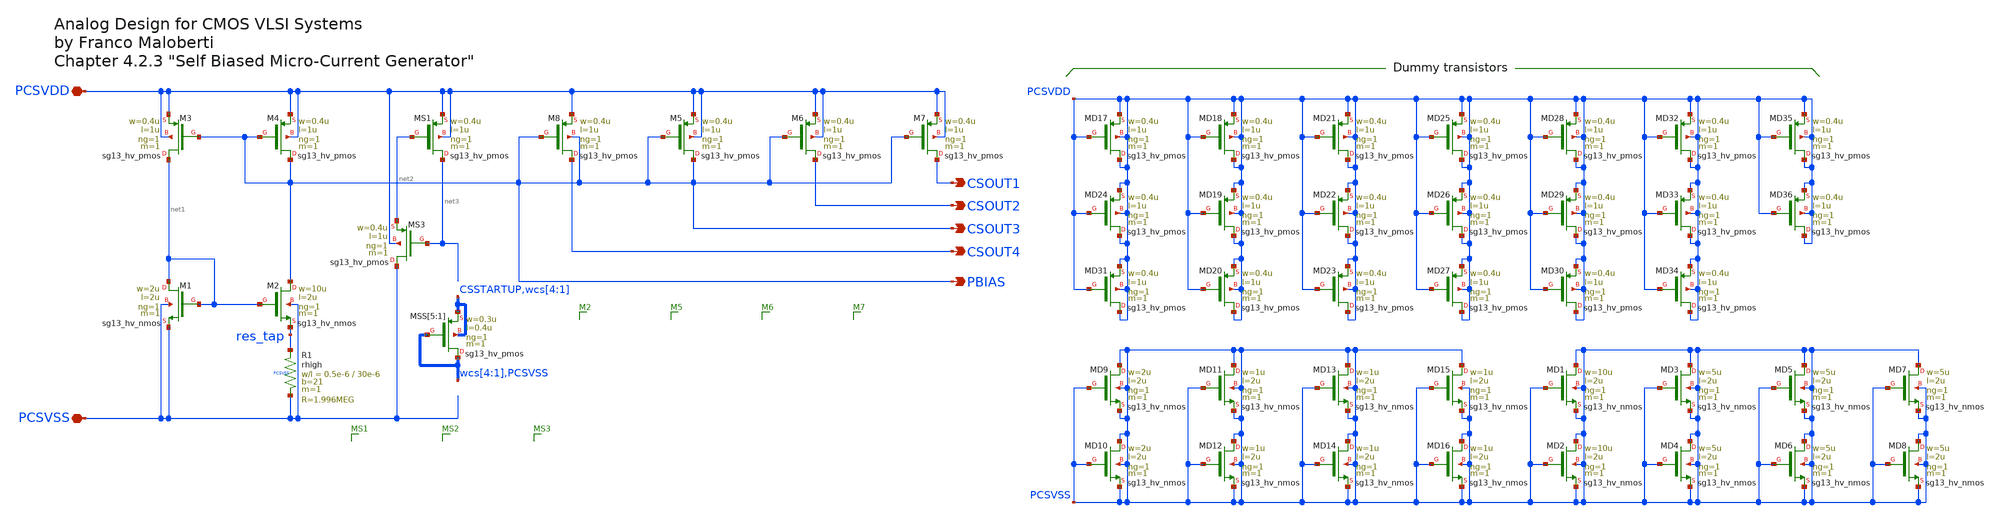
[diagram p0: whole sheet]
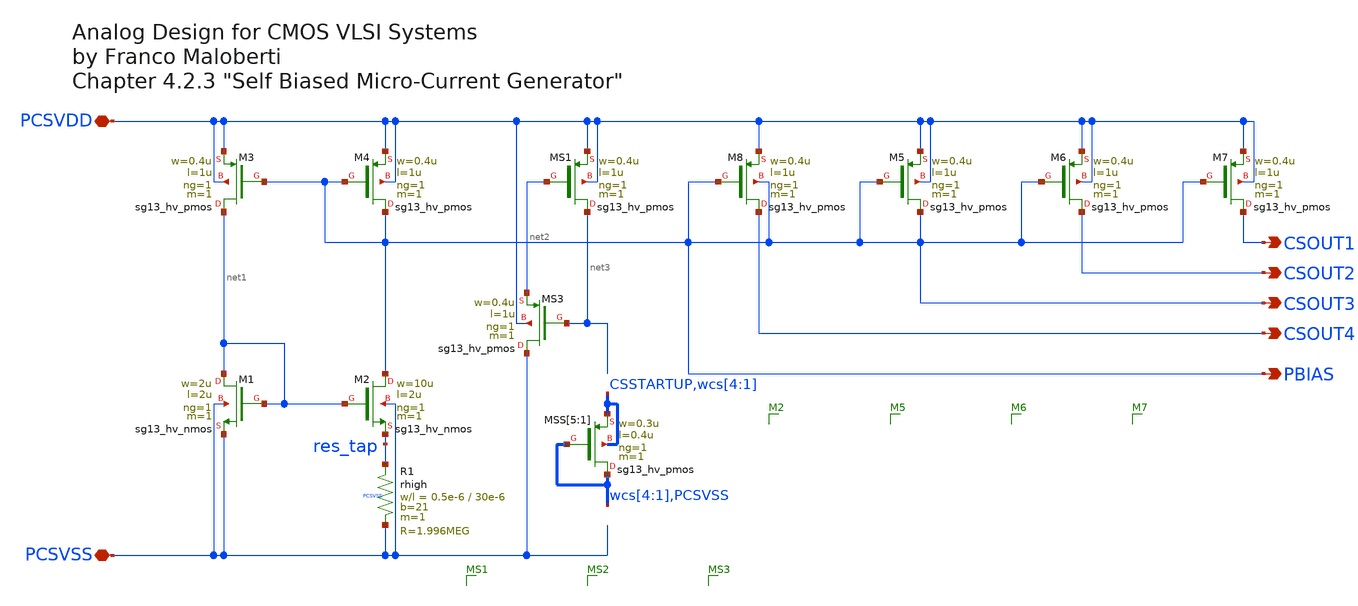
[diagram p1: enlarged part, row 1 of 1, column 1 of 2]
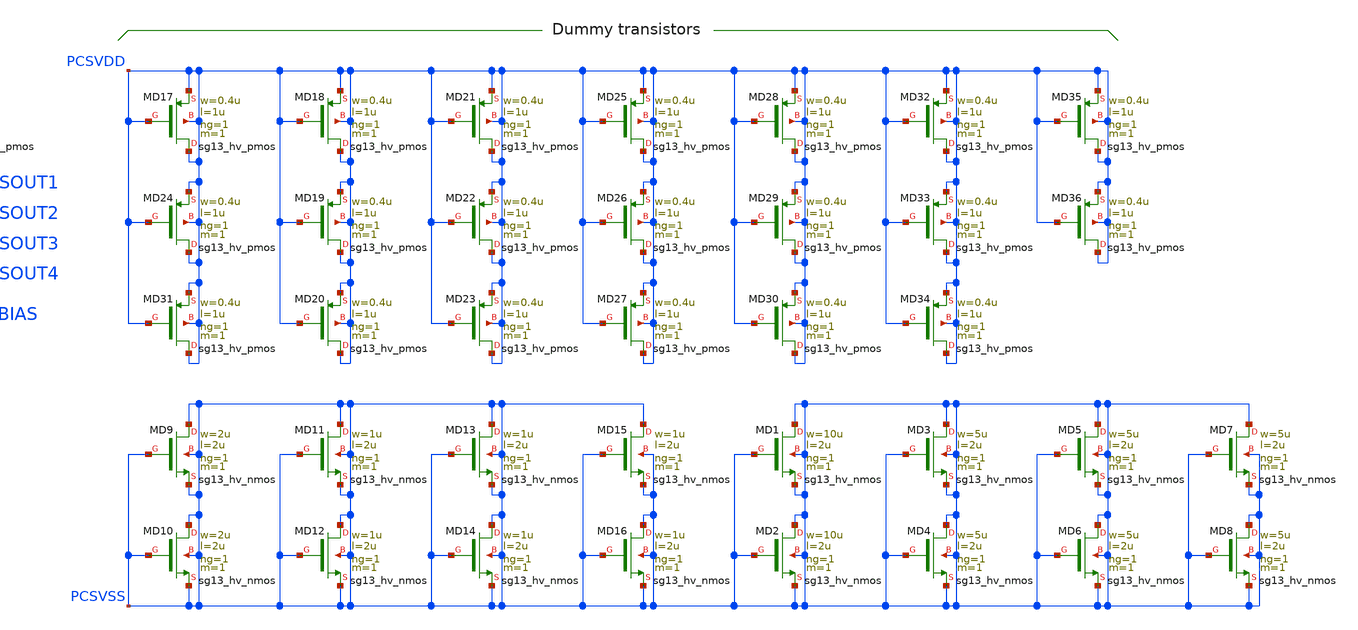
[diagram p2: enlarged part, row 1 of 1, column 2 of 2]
** sch_path: macros/heichips26_FAIf/macros/ptat_current_source/schematic/xschem/ptat_curr_gen_mod1.sch
**.subckt ptat_curr_gen_mod1 PCSVDD PCSVSS CSOUT1 CSOUT2 CSOUT3 PBIAS CSOUT4
*.iopin PCSVDD
*.iopin PCSVSS
*.opin CSOUT1
*.opin CSOUT2
*.opin CSOUT3
*.opin PBIAS
*.opin CSOUT4
XM1 net1 net1 PCSVSS PCSVSS sg13_hv_nmos w=2u l=2u ng=1 m=1 mm_ok=1
XM2 CSOUT3 net1 res_tap PCSVSS sg13_hv_nmos w=10u l=2u ng=1 m=1 mm_ok=1
XM3 net1 CSOUT3 PCSVDD PCSVDD sg13_hv_pmos w=0.4u l=1u ng=1 m=1 mm_ok=1
XM4 CSOUT3 CSOUT3 PCSVDD PCSVDD sg13_hv_pmos w=0.4u l=1u ng=1 m=1 mm_ok=1
XR1 res_tap PCSVSS PCSVSS rhigh w=0.5e-6 l=30e-6 m=1 b=21 mm_ok=1
XM5 CSOUT3 CSOUT3 PCSVDD PCSVDD sg13_hv_pmos w=0.4u l=1u ng=1 m=1 mm_ok=1
XM6 CSOUT2 CSOUT3 PCSVDD PCSVDD sg13_hv_pmos w=0.4u l=1u ng=1 m=1 mm_ok=1
XM7 CSOUT1 CSOUT3 PCSVDD PCSVDD sg13_hv_pmos w=0.4u l=1u ng=1 m=1 mm_ok=1
XMD1 PCSVSS PCSVSS PCSVSS PCSVSS sg13_hv_nmos w=10u l=2u ng=1 m=1 mm_ok=1
XMD2 PCSVSS PCSVSS PCSVSS PCSVSS sg13_hv_nmos w=10u l=2u ng=1 m=1 mm_ok=1
XMD3 PCSVSS PCSVSS PCSVSS PCSVSS sg13_hv_nmos w=5u l=2u ng=1 m=1 mm_ok=1
XMD4 PCSVSS PCSVSS PCSVSS PCSVSS sg13_hv_nmos w=5u l=2u ng=1 m=1 mm_ok=1
XMD5 PCSVSS PCSVSS PCSVSS PCSVSS sg13_hv_nmos w=5u l=2u ng=1 m=1 mm_ok=1
XMD6 PCSVSS PCSVSS PCSVSS PCSVSS sg13_hv_nmos w=5u l=2u ng=1 m=1 mm_ok=1
XMD7 PCSVSS PCSVSS PCSVSS PCSVSS sg13_hv_nmos w=5u l=2u ng=1 m=1 mm_ok=1
XMD8 PCSVSS PCSVSS PCSVSS PCSVSS sg13_hv_nmos w=5u l=2u ng=1 m=1 mm_ok=1
XMD9 PCSVSS PCSVSS PCSVSS PCSVSS sg13_hv_nmos w=2u l=2u ng=1 m=1 mm_ok=1
XMD10 PCSVSS PCSVSS PCSVSS PCSVSS sg13_hv_nmos w=2u l=2u ng=1 m=1 mm_ok=1
XMD11 PCSVSS PCSVSS PCSVSS PCSVSS sg13_hv_nmos w=1u l=2u ng=1 m=1 mm_ok=1
XMD12 PCSVSS PCSVSS PCSVSS PCSVSS sg13_hv_nmos w=1u l=2u ng=1 m=1 mm_ok=1
XMD13 PCSVSS PCSVSS PCSVSS PCSVSS sg13_hv_nmos w=1u l=2u ng=1 m=1 mm_ok=1
XMD14 PCSVSS PCSVSS PCSVSS PCSVSS sg13_hv_nmos w=1u l=2u ng=1 m=1 mm_ok=1
XMD15 PCSVSS PCSVSS PCSVSS PCSVSS sg13_hv_nmos w=1u l=2u ng=1 m=1 mm_ok=1
XMD16 PCSVSS PCSVSS PCSVSS PCSVSS sg13_hv_nmos w=1u l=2u ng=1 m=1 mm_ok=1
XMD17 PCSVDD PCSVDD PCSVDD PCSVDD sg13_hv_pmos w=0.4u l=1u ng=1 m=1 mm_ok=1
XMD24 PCSVDD PCSVDD PCSVDD PCSVDD sg13_hv_pmos w=0.4u l=1u ng=1 m=1 mm_ok=1
XMD31 PCSVDD PCSVDD PCSVDD PCSVDD sg13_hv_pmos w=0.4u l=1u ng=1 m=1 mm_ok=1
XMD18 PCSVDD PCSVDD PCSVDD PCSVDD sg13_hv_pmos w=0.4u l=1u ng=1 m=1 mm_ok=1
XMD19 PCSVDD PCSVDD PCSVDD PCSVDD sg13_hv_pmos w=0.4u l=1u ng=1 m=1 mm_ok=1
XMD20 PCSVDD PCSVDD PCSVDD PCSVDD sg13_hv_pmos w=0.4u l=1u ng=1 m=1 mm_ok=1
XMD21 PCSVDD PCSVDD PCSVDD PCSVDD sg13_hv_pmos w=0.4u l=1u ng=1 m=1 mm_ok=1
XMD22 PCSVDD PCSVDD PCSVDD PCSVDD sg13_hv_pmos w=0.4u l=1u ng=1 m=1 mm_ok=1
XMD23 PCSVDD PCSVDD PCSVDD PCSVDD sg13_hv_pmos w=0.4u l=1u ng=1 m=1 mm_ok=1
XMD25 PCSVDD PCSVDD PCSVDD PCSVDD sg13_hv_pmos w=0.4u l=1u ng=1 m=1 mm_ok=1
XMD26 PCSVDD PCSVDD PCSVDD PCSVDD sg13_hv_pmos w=0.4u l=1u ng=1 m=1 mm_ok=1
XMD27 PCSVDD PCSVDD PCSVDD PCSVDD sg13_hv_pmos w=0.4u l=1u ng=1 m=1 mm_ok=1
XMD28 PCSVDD PCSVDD PCSVDD PCSVDD sg13_hv_pmos w=0.4u l=1u ng=1 m=1 mm_ok=1
XMD29 PCSVDD PCSVDD PCSVDD PCSVDD sg13_hv_pmos w=0.4u l=1u ng=1 m=1 mm_ok=1
XMD30 PCSVDD PCSVDD PCSVDD PCSVDD sg13_hv_pmos w=0.4u l=1u ng=1 m=1 mm_ok=1
XMD32 PCSVDD PCSVDD PCSVDD PCSVDD sg13_hv_pmos w=0.4u l=1u ng=1 m=1 mm_ok=1
XMD33 PCSVDD PCSVDD PCSVDD PCSVDD sg13_hv_pmos w=0.4u l=1u ng=1 m=1 mm_ok=1
XMD34 PCSVDD PCSVDD PCSVDD PCSVDD sg13_hv_pmos w=0.4u l=1u ng=1 m=1 mm_ok=1
XMD35 PCSVDD PCSVDD PCSVDD PCSVDD sg13_hv_pmos w=0.4u l=1u ng=1 m=1 mm_ok=1
XMD36 PCSVDD PCSVDD PCSVDD PCSVDD sg13_hv_pmos w=0.4u l=1u ng=1 m=1 mm_ok=1
XMS1 net3 net2 PCSVDD PCSVDD sg13_hv_pmos w=0.4u l=1u ng=1 m=1 mm_ok=1
XMS3 PCSVSS net3 net2 PCSVDD sg13_hv_pmos w=0.4u l=1u ng=1 m=1 mm_ok=1
XMSS[5] wcs[4] wcs[4] CSSTARTUP CSSTARTUP sg13_hv_pmos w=0.3u l=0.4u ng=1 m=1 mm_ok=1
XMSS[4] wcs[3] wcs[3] wcs[4] wcs[4] sg13_hv_pmos w=0.3u l=0.4u ng=1 m=1 mm_ok=1
XMSS[3] wcs[2] wcs[2] wcs[3] wcs[3] sg13_hv_pmos w=0.3u l=0.4u ng=1 m=1 mm_ok=1
XMSS[2] wcs[1] wcs[1] wcs[2] wcs[2] sg13_hv_pmos w=0.3u l=0.4u ng=1 m=1 mm_ok=1
XMSS[1] PCSVSS PCSVSS wcs[1] wcs[1] sg13_hv_pmos w=0.3u l=0.4u ng=1 m=1 mm_ok=1
XM8 CSOUT4 CSOUT3 PCSVDD CSOUT3 sg13_hv_pmos w=0.4u l=1u ng=1 m=1 mm_ok=1
**.ends
.end
